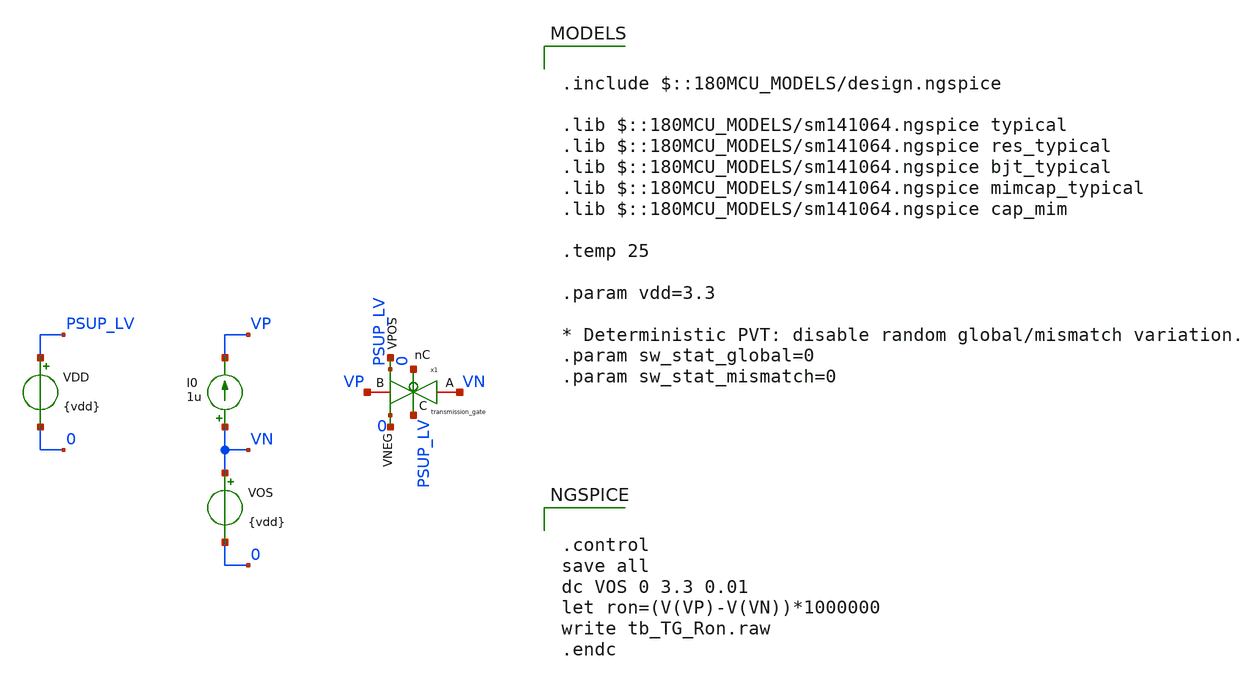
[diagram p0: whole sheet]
** sch_path: xschem/blocks/transmission_gate/tb_TG_Ron.sch
**.subckt tb_TG_Ron
x1 PSUP_LV VN VP 0 net1 net2 transmission_gate
VDD PSUP_LV 0 {vdd}
I0 VN VP 1u
VOS VN 0 {vdd}
**** begin user architecture code

.include $::180MCU_MODELS/design.ngspice

.lib $::180MCU_MODELS/sm141064.ngspice typical
.lib $::180MCU_MODELS/sm141064.ngspice res_typical
.lib $::180MCU_MODELS/sm141064.ngspice bjt_typical
.lib $::180MCU_MODELS/sm141064.ngspice mimcap_typical
.lib $::180MCU_MODELS/sm141064.ngspice cap_mim

.temp 25

.param vdd=3.3

* Deterministic PVT: disable random global/mismatch variation.
.param sw_stat_global=0
.param sw_stat_mismatch=0



.control
save all
dc VOS 0 3.3 0.01
let ron=(V(VP)-V(VN))*1000000
write tb_TG_Ron.raw
.endc


**** end user architecture code
**.ends

* expanding   symbol:  blocks/transmission_gate/transmission_gate.sym # of pins=6
** sym_path: xschem/blocks/transmission_gate/transmission_gate.sym
** sch_path: xschem/blocks/transmission_gate/transmission_gate.sch
.subckt transmission_gate C A B nC VPOS VNEG
*.iopin A
*.iopin B
*.ipin C
*.ipin nC
*.ipin VPOS
*.ipin VNEG
XM3 A C B VNEG nfet_03v3 L=2u W=10u nf=1 ad='int((nf+1)/2) * W/nf * 0.18u' as='int((nf+2)/2) * W/nf * 0.18u'
+ pd='2*int((nf+1)/2) * (W/nf + 0.18u)' ps='2*int((nf+2)/2) * (W/nf + 0.18u)' nrd='0.18u / W' nrs='0.18u / W'
+ sa=0 sb=0 sd=0 m=2
XM4 A nC B VPOS pfet_03v3 L=2u W=10u nf=1 ad='int((nf+1)/2) * W/nf * 0.18u' as='int((nf+2)/2) * W/nf * 0.18u'
+ pd='2*int((nf+1)/2) * (W/nf + 0.18u)' ps='2*int((nf+2)/2) * (W/nf + 0.18u)' nrd='0.18u / W' nrs='0.18u / W'
+ sa=0 sb=0 sd=0 m=4
.ends

.end
